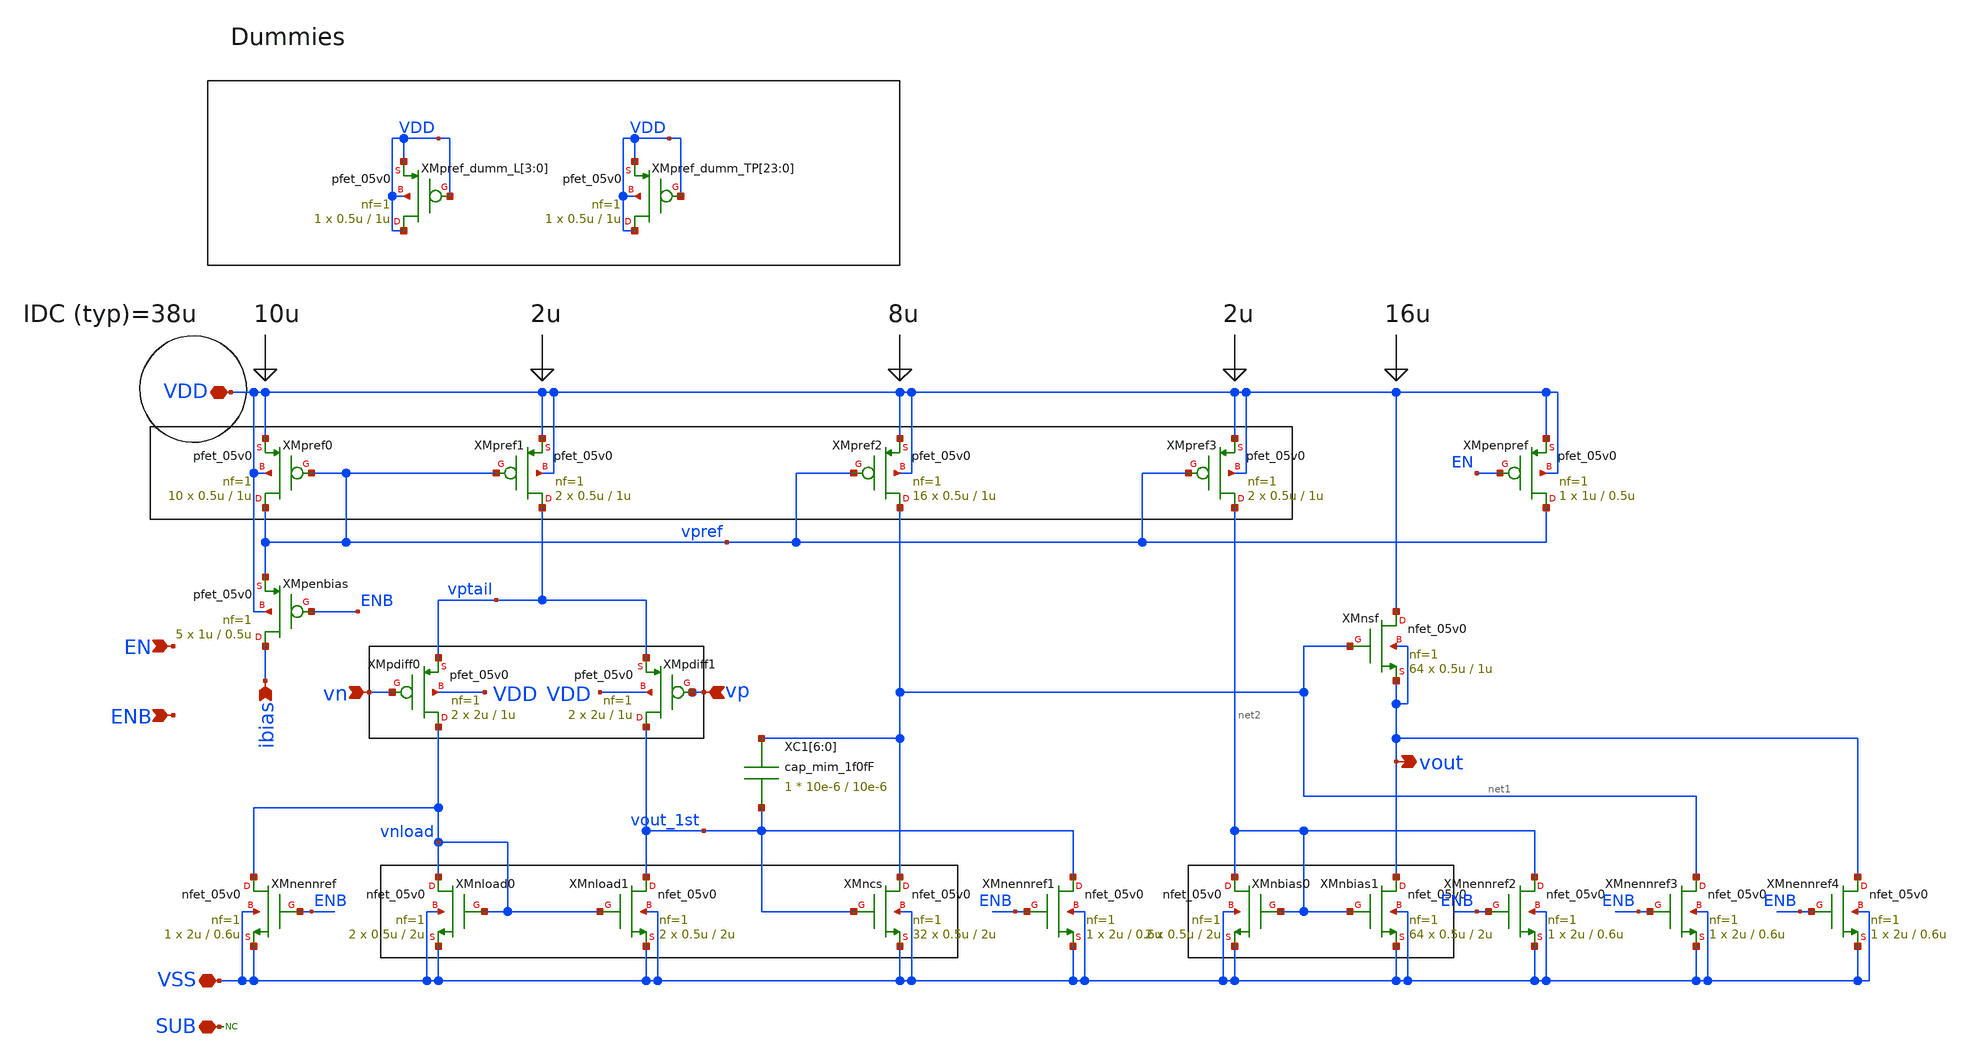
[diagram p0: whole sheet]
** sch_path: designs/libs/core_test/test_buffer/test_buffer.sch
**.subckt test_buffer vn vp vout ibias VDD VSS EN ENB SUB
*.ipin vn
*.ipin vp
*.opin vout
*.ipin ibias
*.iopin VDD
*.iopin VSS
*.ipin EN
*.ipin ENB
*.iopin SUB
XMpref0 vpref vpref VDD VDD pfet_05v0 L=1u W=0.5u nf=1 ad='int((nf+1)/2) * W/nf * 0.18u' as='int((nf+2)/2) * W/nf * 0.18u'
+ pd='2*int((nf+1)/2) * (W/nf + 0.18u)' ps='2*int((nf+2)/2) * (W/nf + 0.18u)' nrd='0.18u / W' nrs='0.18u / W'
+ sa=0 sb=0 sd=0 m=10
XMnload0 vnload vnload VSS VSS nfet_05v0 L=2u W=0.5u nf=1 ad='int((nf+1)/2) * W/nf * 0.18u' as='int((nf+2)/2) * W/nf * 0.18u'
+ pd='2*int((nf+1)/2) * (W/nf + 0.18u)' ps='2*int((nf+2)/2) * (W/nf + 0.18u)' nrd='0.18u / W' nrs='0.18u / W'
+ sa=0 sb=0 sd=0 m=2
XMpref1 vptail vpref VDD VDD pfet_05v0 L=1u W=0.5u nf=1 ad='int((nf+1)/2) * W/nf * 0.18u' as='int((nf+2)/2) * W/nf * 0.18u'
+ pd='2*int((nf+1)/2) * (W/nf + 0.18u)' ps='2*int((nf+2)/2) * (W/nf + 0.18u)' nrd='0.18u / W' nrs='0.18u / W'
+ sa=0 sb=0 sd=0 m=2
XMpref2 net1 vpref VDD VDD pfet_05v0 L=1u W=0.5u nf=1 ad='int((nf+1)/2) * W/nf * 0.18u' as='int((nf+2)/2) * W/nf * 0.18u'
+ pd='2*int((nf+1)/2) * (W/nf + 0.18u)' ps='2*int((nf+2)/2) * (W/nf + 0.18u)' nrd='0.18u / W' nrs='0.18u / W'
+ sa=0 sb=0 sd=0 m=16
XMpdiff0 vnload vn vptail VDD pfet_05v0 L=1u W=2u nf=1 ad='int((nf+1)/2) * W/nf * 0.18u' as='int((nf+2)/2) * W/nf * 0.18u'
+ pd='2*int((nf+1)/2) * (W/nf + 0.18u)' ps='2*int((nf+2)/2) * (W/nf + 0.18u)' nrd='0.18u / W' nrs='0.18u / W'
+ sa=0 sb=0 sd=0 m=2
XMpdiff1 vout_1st vp vptail VDD pfet_05v0 L=1u W=2u nf=1 ad='int((nf+1)/2) * W/nf * 0.18u' as='int((nf+2)/2) * W/nf * 0.18u'
+ pd='2*int((nf+1)/2) * (W/nf + 0.18u)' ps='2*int((nf+2)/2) * (W/nf + 0.18u)' nrd='0.18u / W' nrs='0.18u / W'
+ sa=0 sb=0 sd=0 m=2
XMnload1 vout_1st vnload VSS VSS nfet_05v0 L=2u W=0.5u nf=1 ad='int((nf+1)/2) * W/nf * 0.18u' as='int((nf+2)/2) * W/nf * 0.18u'
+ pd='2*int((nf+1)/2) * (W/nf + 0.18u)' ps='2*int((nf+2)/2) * (W/nf + 0.18u)' nrd='0.18u / W' nrs='0.18u / W'
+ sa=0 sb=0 sd=0 m=2
XMncs net1 vout_1st VSS VSS nfet_05v0 L=2u W=0.5u nf=1 ad='int((nf+1)/2) * W/nf * 0.18u' as='int((nf+2)/2) * W/nf * 0.18u'
+ pd='2*int((nf+1)/2) * (W/nf + 0.18u)' ps='2*int((nf+2)/2) * (W/nf + 0.18u)' nrd='0.18u / W' nrs='0.18u / W'
+ sa=0 sb=0 sd=0 m=32
XMpref_dumm_L[3] VDD VDD VDD VDD pfet_05v0 L=1u W=0.5u nf=1 ad='int((nf+1)/2) * W/nf * 0.18u' as='int((nf+2)/2) * W/nf * 0.18u'
+ pd='2*int((nf+1)/2) * (W/nf + 0.18u)' ps='2*int((nf+2)/2) * (W/nf + 0.18u)' nrd='0.18u / W' nrs='0.18u / W'
+ sa=0 sb=0 sd=0 m=1
XMpref_dumm_L[2] VDD VDD VDD VDD pfet_05v0 L=1u W=0.5u nf=1 ad='int((nf+1)/2) * W/nf * 0.18u' as='int((nf+2)/2) * W/nf * 0.18u'
+ pd='2*int((nf+1)/2) * (W/nf + 0.18u)' ps='2*int((nf+2)/2) * (W/nf + 0.18u)' nrd='0.18u / W' nrs='0.18u / W'
+ sa=0 sb=0 sd=0 m=1
XMpref_dumm_L[1] VDD VDD VDD VDD pfet_05v0 L=1u W=0.5u nf=1 ad='int((nf+1)/2) * W/nf * 0.18u' as='int((nf+2)/2) * W/nf * 0.18u'
+ pd='2*int((nf+1)/2) * (W/nf + 0.18u)' ps='2*int((nf+2)/2) * (W/nf + 0.18u)' nrd='0.18u / W' nrs='0.18u / W'
+ sa=0 sb=0 sd=0 m=1
XMpref_dumm_L[0] VDD VDD VDD VDD pfet_05v0 L=1u W=0.5u nf=1 ad='int((nf+1)/2) * W/nf * 0.18u' as='int((nf+2)/2) * W/nf * 0.18u'
+ pd='2*int((nf+1)/2) * (W/nf + 0.18u)' ps='2*int((nf+2)/2) * (W/nf + 0.18u)' nrd='0.18u / W' nrs='0.18u / W'
+ sa=0 sb=0 sd=0 m=1
XMpref_dumm_TP[23] VDD VDD VDD VDD pfet_05v0 L=1u W=0.5u nf=1 ad='int((nf+1)/2) * W/nf * 0.18u' as='int((nf+2)/2) * W/nf * 0.18u'
+ pd='2*int((nf+1)/2) * (W/nf + 0.18u)' ps='2*int((nf+2)/2) * (W/nf + 0.18u)' nrd='0.18u / W' nrs='0.18u / W'
+ sa=0 sb=0 sd=0 m=1
XMpref_dumm_TP[22] VDD VDD VDD VDD pfet_05v0 L=1u W=0.5u nf=1 ad='int((nf+1)/2) * W/nf * 0.18u' as='int((nf+2)/2) * W/nf * 0.18u'
+ pd='2*int((nf+1)/2) * (W/nf + 0.18u)' ps='2*int((nf+2)/2) * (W/nf + 0.18u)' nrd='0.18u / W' nrs='0.18u / W'
+ sa=0 sb=0 sd=0 m=1
XMpref_dumm_TP[21] VDD VDD VDD VDD pfet_05v0 L=1u W=0.5u nf=1 ad='int((nf+1)/2) * W/nf * 0.18u' as='int((nf+2)/2) * W/nf * 0.18u'
+ pd='2*int((nf+1)/2) * (W/nf + 0.18u)' ps='2*int((nf+2)/2) * (W/nf + 0.18u)' nrd='0.18u / W' nrs='0.18u / W'
+ sa=0 sb=0 sd=0 m=1
XMpref_dumm_TP[20] VDD VDD VDD VDD pfet_05v0 L=1u W=0.5u nf=1 ad='int((nf+1)/2) * W/nf * 0.18u' as='int((nf+2)/2) * W/nf * 0.18u'
+ pd='2*int((nf+1)/2) * (W/nf + 0.18u)' ps='2*int((nf+2)/2) * (W/nf + 0.18u)' nrd='0.18u / W' nrs='0.18u / W'
+ sa=0 sb=0 sd=0 m=1
XMpref_dumm_TP[19] VDD VDD VDD VDD pfet_05v0 L=1u W=0.5u nf=1 ad='int((nf+1)/2) * W/nf * 0.18u' as='int((nf+2)/2) * W/nf * 0.18u'
+ pd='2*int((nf+1)/2) * (W/nf + 0.18u)' ps='2*int((nf+2)/2) * (W/nf + 0.18u)' nrd='0.18u / W' nrs='0.18u / W'
+ sa=0 sb=0 sd=0 m=1
XMpref_dumm_TP[18] VDD VDD VDD VDD pfet_05v0 L=1u W=0.5u nf=1 ad='int((nf+1)/2) * W/nf * 0.18u' as='int((nf+2)/2) * W/nf * 0.18u'
+ pd='2*int((nf+1)/2) * (W/nf + 0.18u)' ps='2*int((nf+2)/2) * (W/nf + 0.18u)' nrd='0.18u / W' nrs='0.18u / W'
+ sa=0 sb=0 sd=0 m=1
XMpref_dumm_TP[17] VDD VDD VDD VDD pfet_05v0 L=1u W=0.5u nf=1 ad='int((nf+1)/2) * W/nf * 0.18u' as='int((nf+2)/2) * W/nf * 0.18u'
+ pd='2*int((nf+1)/2) * (W/nf + 0.18u)' ps='2*int((nf+2)/2) * (W/nf + 0.18u)' nrd='0.18u / W' nrs='0.18u / W'
+ sa=0 sb=0 sd=0 m=1
XMpref_dumm_TP[16] VDD VDD VDD VDD pfet_05v0 L=1u W=0.5u nf=1 ad='int((nf+1)/2) * W/nf * 0.18u' as='int((nf+2)/2) * W/nf * 0.18u'
+ pd='2*int((nf+1)/2) * (W/nf + 0.18u)' ps='2*int((nf+2)/2) * (W/nf + 0.18u)' nrd='0.18u / W' nrs='0.18u / W'
+ sa=0 sb=0 sd=0 m=1
XMpref_dumm_TP[15] VDD VDD VDD VDD pfet_05v0 L=1u W=0.5u nf=1 ad='int((nf+1)/2) * W/nf * 0.18u' as='int((nf+2)/2) * W/nf * 0.18u'
+ pd='2*int((nf+1)/2) * (W/nf + 0.18u)' ps='2*int((nf+2)/2) * (W/nf + 0.18u)' nrd='0.18u / W' nrs='0.18u / W'
+ sa=0 sb=0 sd=0 m=1
XMpref_dumm_TP[14] VDD VDD VDD VDD pfet_05v0 L=1u W=0.5u nf=1 ad='int((nf+1)/2) * W/nf * 0.18u' as='int((nf+2)/2) * W/nf * 0.18u'
+ pd='2*int((nf+1)/2) * (W/nf + 0.18u)' ps='2*int((nf+2)/2) * (W/nf + 0.18u)' nrd='0.18u / W' nrs='0.18u / W'
+ sa=0 sb=0 sd=0 m=1
XMpref_dumm_TP[13] VDD VDD VDD VDD pfet_05v0 L=1u W=0.5u nf=1 ad='int((nf+1)/2) * W/nf * 0.18u' as='int((nf+2)/2) * W/nf * 0.18u'
+ pd='2*int((nf+1)/2) * (W/nf + 0.18u)' ps='2*int((nf+2)/2) * (W/nf + 0.18u)' nrd='0.18u / W' nrs='0.18u / W'
+ sa=0 sb=0 sd=0 m=1
XMpref_dumm_TP[12] VDD VDD VDD VDD pfet_05v0 L=1u W=0.5u nf=1 ad='int((nf+1)/2) * W/nf * 0.18u' as='int((nf+2)/2) * W/nf * 0.18u'
+ pd='2*int((nf+1)/2) * (W/nf + 0.18u)' ps='2*int((nf+2)/2) * (W/nf + 0.18u)' nrd='0.18u / W' nrs='0.18u / W'
+ sa=0 sb=0 sd=0 m=1
XMpref_dumm_TP[11] VDD VDD VDD VDD pfet_05v0 L=1u W=0.5u nf=1 ad='int((nf+1)/2) * W/nf * 0.18u' as='int((nf+2)/2) * W/nf * 0.18u'
+ pd='2*int((nf+1)/2) * (W/nf + 0.18u)' ps='2*int((nf+2)/2) * (W/nf + 0.18u)' nrd='0.18u / W' nrs='0.18u / W'
+ sa=0 sb=0 sd=0 m=1
XMpref_dumm_TP[10] VDD VDD VDD VDD pfet_05v0 L=1u W=0.5u nf=1 ad='int((nf+1)/2) * W/nf * 0.18u' as='int((nf+2)/2) * W/nf * 0.18u'
+ pd='2*int((nf+1)/2) * (W/nf + 0.18u)' ps='2*int((nf+2)/2) * (W/nf + 0.18u)' nrd='0.18u / W' nrs='0.18u / W'
+ sa=0 sb=0 sd=0 m=1
XMpref_dumm_TP[9] VDD VDD VDD VDD pfet_05v0 L=1u W=0.5u nf=1 ad='int((nf+1)/2) * W/nf * 0.18u' as='int((nf+2)/2) * W/nf * 0.18u'
+ pd='2*int((nf+1)/2) * (W/nf + 0.18u)' ps='2*int((nf+2)/2) * (W/nf + 0.18u)' nrd='0.18u / W' nrs='0.18u / W'
+ sa=0 sb=0 sd=0 m=1
XMpref_dumm_TP[8] VDD VDD VDD VDD pfet_05v0 L=1u W=0.5u nf=1 ad='int((nf+1)/2) * W/nf * 0.18u' as='int((nf+2)/2) * W/nf * 0.18u'
+ pd='2*int((nf+1)/2) * (W/nf + 0.18u)' ps='2*int((nf+2)/2) * (W/nf + 0.18u)' nrd='0.18u / W' nrs='0.18u / W'
+ sa=0 sb=0 sd=0 m=1
XMpref_dumm_TP[7] VDD VDD VDD VDD pfet_05v0 L=1u W=0.5u nf=1 ad='int((nf+1)/2) * W/nf * 0.18u' as='int((nf+2)/2) * W/nf * 0.18u'
+ pd='2*int((nf+1)/2) * (W/nf + 0.18u)' ps='2*int((nf+2)/2) * (W/nf + 0.18u)' nrd='0.18u / W' nrs='0.18u / W'
+ sa=0 sb=0 sd=0 m=1
XMpref_dumm_TP[6] VDD VDD VDD VDD pfet_05v0 L=1u W=0.5u nf=1 ad='int((nf+1)/2) * W/nf * 0.18u' as='int((nf+2)/2) * W/nf * 0.18u'
+ pd='2*int((nf+1)/2) * (W/nf + 0.18u)' ps='2*int((nf+2)/2) * (W/nf + 0.18u)' nrd='0.18u / W' nrs='0.18u / W'
+ sa=0 sb=0 sd=0 m=1
XMpref_dumm_TP[5] VDD VDD VDD VDD pfet_05v0 L=1u W=0.5u nf=1 ad='int((nf+1)/2) * W/nf * 0.18u' as='int((nf+2)/2) * W/nf * 0.18u'
+ pd='2*int((nf+1)/2) * (W/nf + 0.18u)' ps='2*int((nf+2)/2) * (W/nf + 0.18u)' nrd='0.18u / W' nrs='0.18u / W'
+ sa=0 sb=0 sd=0 m=1
XMpref_dumm_TP[4] VDD VDD VDD VDD pfet_05v0 L=1u W=0.5u nf=1 ad='int((nf+1)/2) * W/nf * 0.18u' as='int((nf+2)/2) * W/nf * 0.18u'
+ pd='2*int((nf+1)/2) * (W/nf + 0.18u)' ps='2*int((nf+2)/2) * (W/nf + 0.18u)' nrd='0.18u / W' nrs='0.18u / W'
+ sa=0 sb=0 sd=0 m=1
XMpref_dumm_TP[3] VDD VDD VDD VDD pfet_05v0 L=1u W=0.5u nf=1 ad='int((nf+1)/2) * W/nf * 0.18u' as='int((nf+2)/2) * W/nf * 0.18u'
+ pd='2*int((nf+1)/2) * (W/nf + 0.18u)' ps='2*int((nf+2)/2) * (W/nf + 0.18u)' nrd='0.18u / W' nrs='0.18u / W'
+ sa=0 sb=0 sd=0 m=1
XMpref_dumm_TP[2] VDD VDD VDD VDD pfet_05v0 L=1u W=0.5u nf=1 ad='int((nf+1)/2) * W/nf * 0.18u' as='int((nf+2)/2) * W/nf * 0.18u'
+ pd='2*int((nf+1)/2) * (W/nf + 0.18u)' ps='2*int((nf+2)/2) * (W/nf + 0.18u)' nrd='0.18u / W' nrs='0.18u / W'
+ sa=0 sb=0 sd=0 m=1
XMpref_dumm_TP[1] VDD VDD VDD VDD pfet_05v0 L=1u W=0.5u nf=1 ad='int((nf+1)/2) * W/nf * 0.18u' as='int((nf+2)/2) * W/nf * 0.18u'
+ pd='2*int((nf+1)/2) * (W/nf + 0.18u)' ps='2*int((nf+2)/2) * (W/nf + 0.18u)' nrd='0.18u / W' nrs='0.18u / W'
+ sa=0 sb=0 sd=0 m=1
XMpref_dumm_TP[0] VDD VDD VDD VDD pfet_05v0 L=1u W=0.5u nf=1 ad='int((nf+1)/2) * W/nf * 0.18u' as='int((nf+2)/2) * W/nf * 0.18u'
+ pd='2*int((nf+1)/2) * (W/nf + 0.18u)' ps='2*int((nf+2)/2) * (W/nf + 0.18u)' nrd='0.18u / W' nrs='0.18u / W'
+ sa=0 sb=0 sd=0 m=1
XMpenpref vpref EN VDD VDD pfet_05v0 L=0.5u W=1u nf=1 ad='int((nf+1)/2) * W/nf * 0.18u' as='int((nf+2)/2) * W/nf * 0.18u'
+ pd='2*int((nf+1)/2) * (W/nf + 0.18u)' ps='2*int((nf+2)/2) * (W/nf + 0.18u)' nrd='0.18u / W' nrs='0.18u / W'
+ sa=0 sb=0 sd=0 m=1
XMpenbias ibias ENB vpref VDD pfet_05v0 L=0.5u W=1u nf=1 ad='int((nf+1)/2) * W/nf * 0.18u' as='int((nf+2)/2) * W/nf * 0.18u'
+ pd='2*int((nf+1)/2) * (W/nf + 0.18u)' ps='2*int((nf+2)/2) * (W/nf + 0.18u)' nrd='0.18u / W' nrs='0.18u / W'
+ sa=0 sb=0 sd=0 m=5
XMnennref vnload ENB VSS VSS nfet_05v0 L=0.6u W=2u nf=1 ad='int((nf+1)/2) * W/nf * 0.18u' as='int((nf+2)/2) * W/nf * 0.18u'
+ pd='2*int((nf+1)/2) * (W/nf + 0.18u)' ps='2*int((nf+2)/2) * (W/nf + 0.18u)' nrd='0.18u / W' nrs='0.18u / W'
+ sa=0 sb=0 sd=0 m=1
XMnennref1 vout_1st ENB VSS VSS nfet_05v0 L=0.6u W=2u nf=1 ad='int((nf+1)/2) * W/nf * 0.18u' as='int((nf+2)/2) * W/nf * 0.18u'
+ pd='2*int((nf+1)/2) * (W/nf + 0.18u)' ps='2*int((nf+2)/2) * (W/nf + 0.18u)' nrd='0.18u / W' nrs='0.18u / W'
+ sa=0 sb=0 sd=0 m=1
* noconn SUB
XMpref3 net2 vpref VDD VDD pfet_05v0 L=1u W=0.5u nf=1 ad='int((nf+1)/2) * W/nf * 0.18u' as='int((nf+2)/2) * W/nf * 0.18u'
+ pd='2*int((nf+1)/2) * (W/nf + 0.18u)' ps='2*int((nf+2)/2) * (W/nf + 0.18u)' nrd='0.18u / W' nrs='0.18u / W'
+ sa=0 sb=0 sd=0 m=2
XMnbias0 net2 net2 VSS VSS nfet_05v0 L=2u W=0.5u nf=1 ad='int((nf+1)/2) * W/nf * 0.18u' as='int((nf+2)/2) * W/nf * 0.18u'
+ pd='2*int((nf+1)/2) * (W/nf + 0.18u)' ps='2*int((nf+2)/2) * (W/nf + 0.18u)' nrd='0.18u / W' nrs='0.18u / W'
+ sa=0 sb=0 sd=0 m=2
XMnbias1 vout net2 VSS VSS nfet_05v0 L=2u W=0.5u nf=1 ad='int((nf+1)/2) * W/nf * 0.18u' as='int((nf+2)/2) * W/nf * 0.18u'
+ pd='2*int((nf+1)/2) * (W/nf + 0.18u)' ps='2*int((nf+2)/2) * (W/nf + 0.18u)' nrd='0.18u / W' nrs='0.18u / W'
+ sa=0 sb=0 sd=0 m=64
XMnsf VDD net1 vout vout nfet_05v0 L=1u W=0.5u nf=1 ad='int((nf+1)/2) * W/nf * 0.18u' as='int((nf+2)/2) * W/nf * 0.18u'
+ pd='2*int((nf+1)/2) * (W/nf + 0.18u)' ps='2*int((nf+2)/2) * (W/nf + 0.18u)' nrd='0.18u / W' nrs='0.18u / W'
+ sa=0 sb=0 sd=0 m=64
XMnennref2 net2 ENB VSS VSS nfet_05v0 L=0.6u W=2u nf=1 ad='int((nf+1)/2) * W/nf * 0.18u' as='int((nf+2)/2) * W/nf * 0.18u'
+ pd='2*int((nf+1)/2) * (W/nf + 0.18u)' ps='2*int((nf+2)/2) * (W/nf + 0.18u)' nrd='0.18u / W' nrs='0.18u / W'
+ sa=0 sb=0 sd=0 m=1
XMnennref3 net1 ENB VSS VSS nfet_05v0 L=0.6u W=2u nf=1 ad='int((nf+1)/2) * W/nf * 0.18u' as='int((nf+2)/2) * W/nf * 0.18u'
+ pd='2*int((nf+1)/2) * (W/nf + 0.18u)' ps='2*int((nf+2)/2) * (W/nf + 0.18u)' nrd='0.18u / W' nrs='0.18u / W'
+ sa=0 sb=0 sd=0 m=1
XMnennref4 vout ENB VSS VSS nfet_05v0 L=0.6u W=2u nf=1 ad='int((nf+1)/2) * W/nf * 0.18u' as='int((nf+2)/2) * W/nf * 0.18u'
+ pd='2*int((nf+1)/2) * (W/nf + 0.18u)' ps='2*int((nf+2)/2) * (W/nf + 0.18u)' nrd='0.18u / W' nrs='0.18u / W'
+ sa=0 sb=0 sd=0 m=1
XC1[6] net1 vout_1st cap_mim_1f0fF c_width=10e-6 c_length=10e-6 m=1
XC1[5] net1 vout_1st cap_mim_1f0fF c_width=10e-6 c_length=10e-6 m=1
XC1[4] net1 vout_1st cap_mim_1f0fF c_width=10e-6 c_length=10e-6 m=1
XC1[3] net1 vout_1st cap_mim_1f0fF c_width=10e-6 c_length=10e-6 m=1
XC1[2] net1 vout_1st cap_mim_1f0fF c_width=10e-6 c_length=10e-6 m=1
XC1[1] net1 vout_1st cap_mim_1f0fF c_width=10e-6 c_length=10e-6 m=1
XC1[0] net1 vout_1st cap_mim_1f0fF c_width=10e-6 c_length=10e-6 m=1
**.ends
.end
